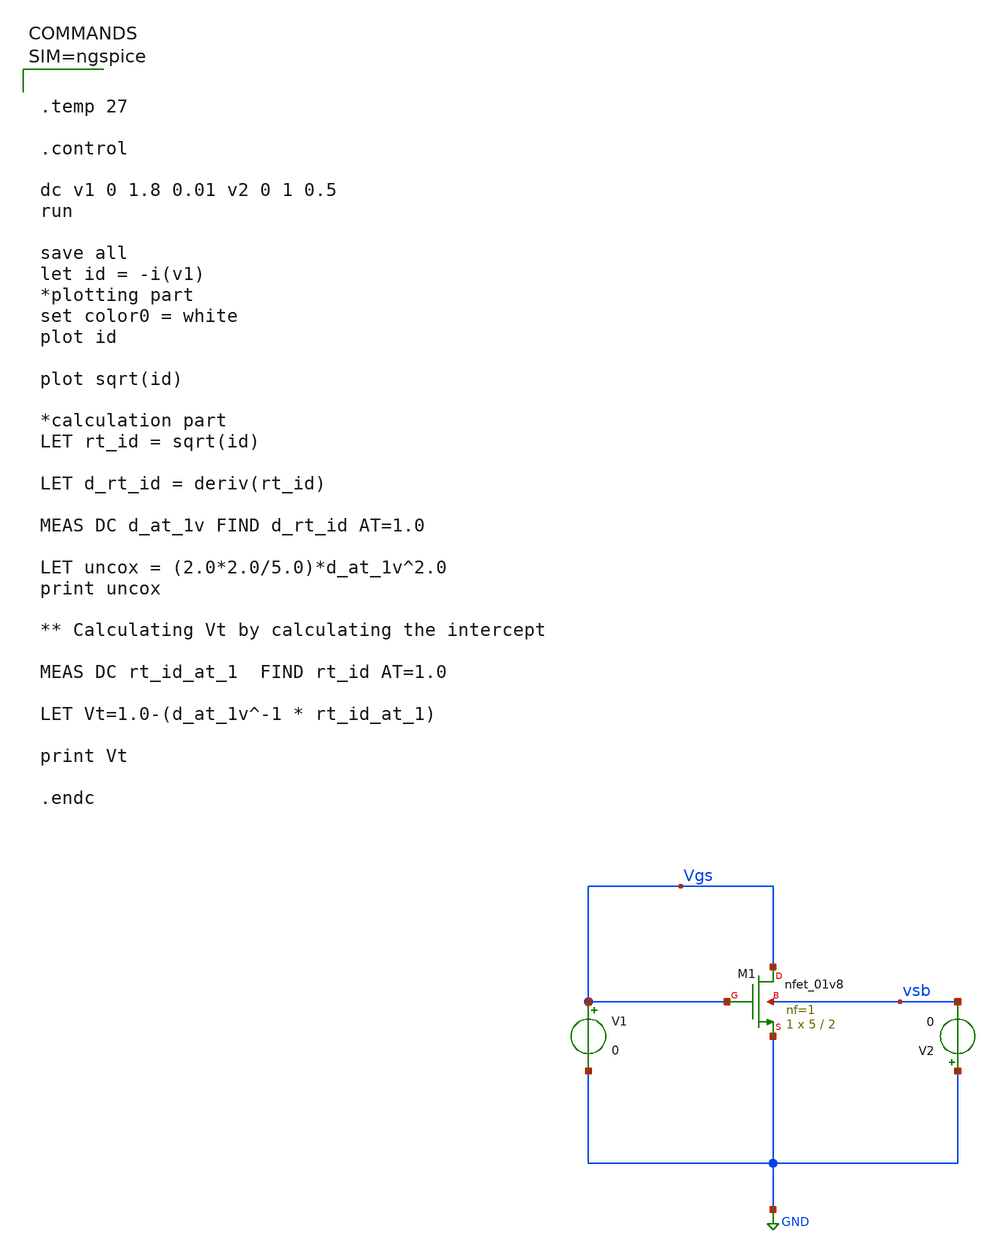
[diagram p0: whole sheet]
** sch_path: sch/Nmos_parameter_extract.sch
**.subckt Nmos_parameter_extract
XM1 Vgs Vgs GND vsb sky130_fd_pr__nfet_01v8 L=2 W=5 nf=1 ad='int((1 + 1)/2) * 5 / 1 * 0.29' as='int((1 + 2)/2) * 5 / 1 * 0.29'
+ pd='2*int((1 + 1)/2) * (5 / 1 + 0.29)' ps='2*int((1 + 2)/2) * (5 / 1 + 0.29)' nrd='0.29 / 5 ' nrs='0.29 / 5 '
+ sa=0 sb=0 sd=0 mult=1 m=1
V1 Vgs GND 0
V2 GND vsb 0
**** begin user architecture code

** opencircuitdesign pdks install
.lib $::SKYWATER_MODELS/sky130.lib.spice tt




.temp 27

.control

dc v1 0 1.8 0.01 v2 0 1 0.5
run

save all
let id = -i(v1)
*plotting part
set color0 = white
plot id

plot sqrt(id)

*calculation part
LET rt_id = sqrt(id)

LET d_rt_id = deriv(rt_id)

MEAS DC d_at_1v FIND d_rt_id AT=1.0

LET uncox = (2.0*2.0/5.0)*d_at_1v^2.0
print uncox

** Calculating Vt by calculating the intercept

MEAS DC rt_id_at_1  FIND rt_id AT=1.0

LET Vt=1.0-(d_at_1v^-1 * rt_id_at_1)

print Vt

.endc



**** end user architecture code
**.ends
.GLOBAL GND
.end
